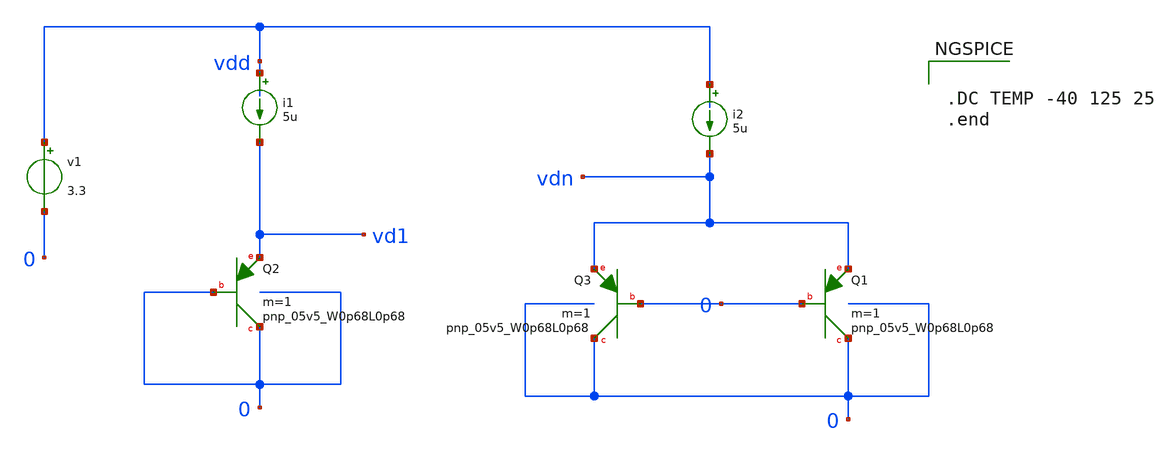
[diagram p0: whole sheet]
** sch_path: Bandgap/PTAT.sch
**.subckt PTAT
i1 vdd vd1 5u
v1 vdd 0 3.3
XQ2 0 0 vd1 sky130_fd_pr__pnp_05v5_W0p68L0p68 m=1
i2 vdd vdn 5u
XQ1 0 0 vdn sky130_fd_pr__pnp_05v5_W0p68L0p68 m=1
XQ3 0 0 vdn sky130_fd_pr__pnp_05v5_W0p68L0p68 m=1
**** begin user architecture code

.include $::SKYWATER_MODELS/cells/nfet_01v8/sky130_fd_pr__nfet_01v8__tt.corner.spice
.include $::SKYWATER_MODELS/cells/nfet_01v8_lvt/sky130_fd_pr__nfet_01v8_lvt__tt.corner.spice
.include $::SKYWATER_MODELS/cells/pfet_01v8/sky130_fd_pr__pfet_01v8__tt.corner.spice
.include $::SKYWATER_MODELS/cells/nfet_03v3_nvt/sky130_fd_pr__nfet_03v3_nvt__tt.corner.spice
.include $::SKYWATER_MODELS/cells/nfet_05v0_nvt/sky130_fd_pr__nfet_05v0_nvt__tt.corner.spice
.include $::SKYWATER_MODELS/cells/esd_nfet_01v8/sky130_fd_pr__esd_nfet_01v8__tt.corner.spice
.include $::SKYWATER_MODELS/cells/pfet_01v8_lvt/sky130_fd_pr__pfet_01v8_lvt__tt.corner.spice
.include $::SKYWATER_MODELS/cells/pfet_01v8_hvt/sky130_fd_pr__pfet_01v8_hvt__tt.corner.spice
.include $::SKYWATER_MODELS/cells/esd_pfet_g5v0d10v5/sky130_fd_pr__esd_pfet_g5v0d10v5__tt.corner.spice
.include $::SKYWATER_MODELS/cells/pfet_g5v0d10v5/sky130_fd_pr__pfet_g5v0d10v5__tt.corner.spice
.include $::SKYWATER_MODELS/cells/pfet_g5v0d16v0/sky130_fd_pr__pfet_g5v0d16v0__tt.corner.spice
.include $::SKYWATER_MODELS/cells/nfet_g5v0d10v5/sky130_fd_pr__nfet_g5v0d10v5__tt.corner.spice
.include $::SKYWATER_MODELS/cells/nfet_g5v0d16v0/sky130_fd_pr__nfet_g5v0d16v0__tt_discrete.corner.spice
.include $::SKYWATER_MODELS/cells/esd_nfet_g5v0d10v5/sky130_fd_pr__esd_nfet_g5v0d10v5__tt.corner.spice
.include $::SKYWATER_MODELS/models/corners/tt/nonfet.spice
* Mismatch parameters
.include $::SKYWATER_MODELS/cells/nfet_01v8/sky130_fd_pr__nfet_01v8__mismatch.corner.spice
.include $::SKYWATER_MODELS/cells/pfet_01v8/sky130_fd_pr__pfet_01v8__mismatch.corner.spice
.include $::SKYWATER_MODELS/cells/nfet_01v8_lvt/sky130_fd_pr__nfet_01v8_lvt__mismatch.corner.spice
.include $::SKYWATER_MODELS/cells/pfet_01v8_lvt/sky130_fd_pr__pfet_01v8_lvt__mismatch.corner.spice
.include $::SKYWATER_MODELS/cells/pfet_01v8_hvt/sky130_fd_pr__pfet_01v8_hvt__mismatch.corner.spice
.include $::SKYWATER_MODELS/cells/nfet_g5v0d10v5/sky130_fd_pr__nfet_g5v0d10v5__mismatch.corner.spice
.include $::SKYWATER_MODELS/cells/pfet_g5v0d10v5/sky130_fd_pr__pfet_g5v0d10v5__mismatch.corner.spice
.include $::SKYWATER_MODELS/cells/nfet_05v0_nvt/sky130_fd_pr__nfet_05v0_nvt__mismatch.corner.spice
.include $::SKYWATER_MODELS/cells/nfet_03v3_nvt/sky130_fd_pr__nfet_03v3_nvt__mismatch.corner.spice
* Resistor$::SKYWATER_MODELS/Capacitor
.include $::SKYWATER_MODELS/models/r+c/res_typical__cap_typical.spice
.include $::SKYWATER_MODELS/models/r+c/res_typical__cap_typical__lin.spice
* Special cells
.include $::SKYWATER_MODELS/models/corners/tt/specialized_cells.spice
* All models
.include $::SKYWATER_MODELS/models/all.spice
* Corner
.include $::SKYWATER_MODELS/models/corners/tt/rf.spice



.DC TEMP -40 125 25
.end


**** end user architecture code
**.ends
.end
